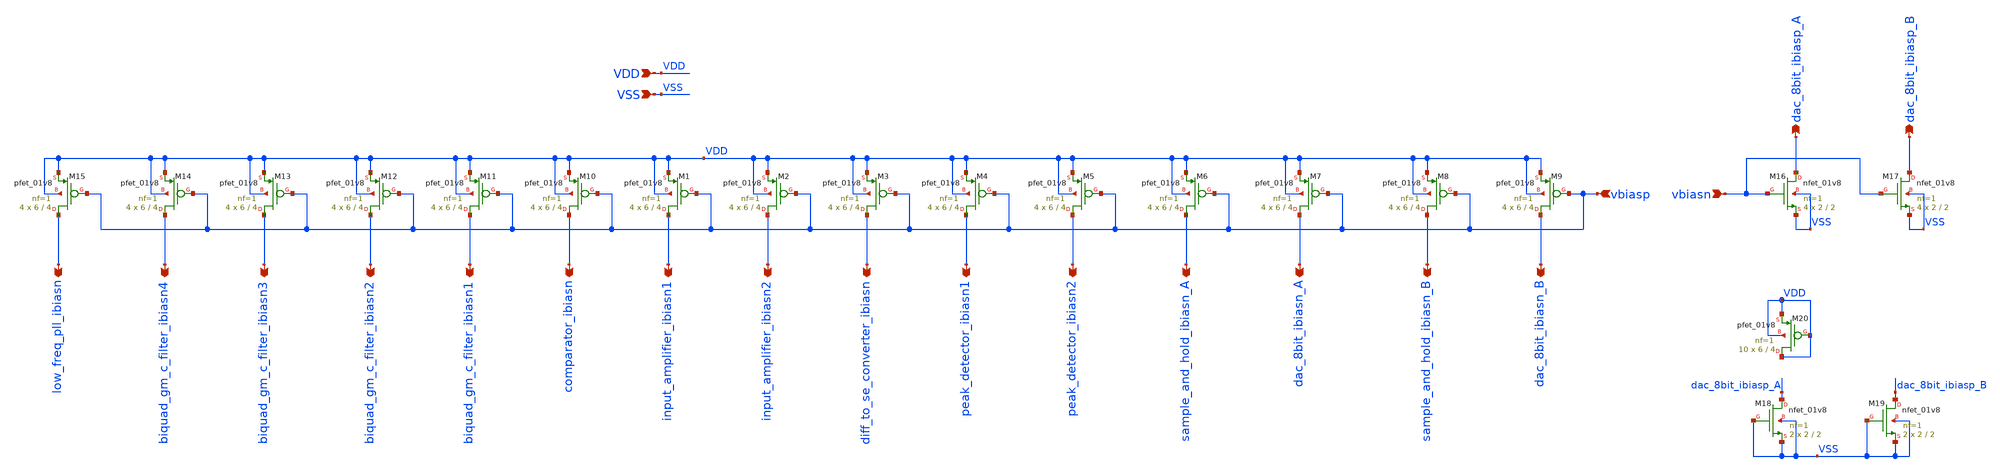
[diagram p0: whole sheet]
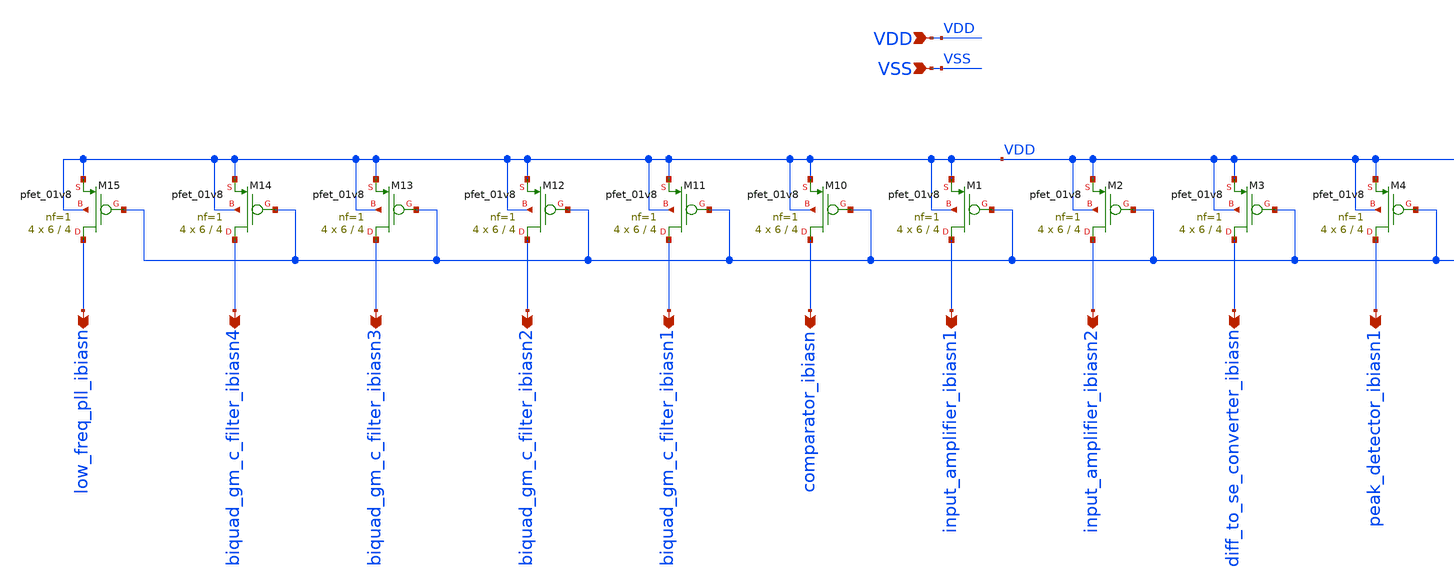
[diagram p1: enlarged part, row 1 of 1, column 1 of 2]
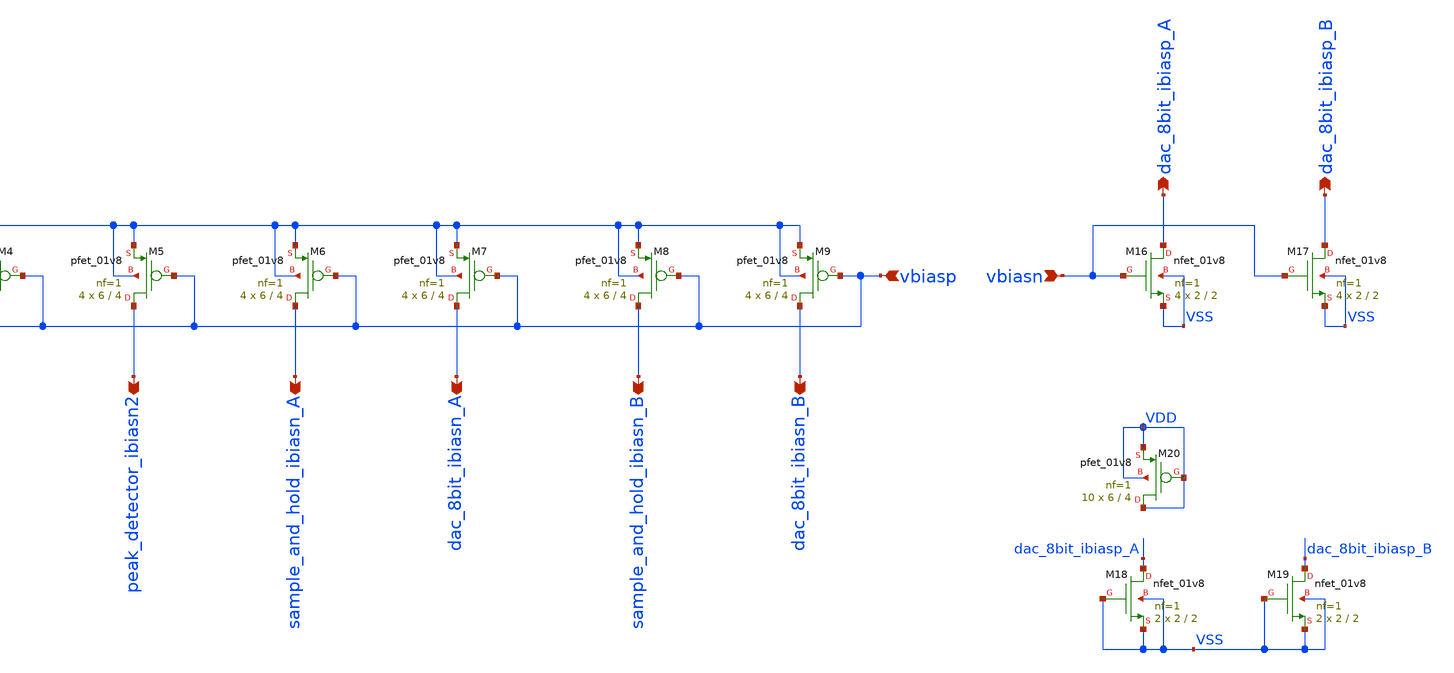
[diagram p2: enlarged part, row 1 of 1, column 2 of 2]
** sch_path: designs/bias_current_distribution_lvs.sch
* Copyright 2020 Stefan Frederik Schippers
* Licensed under the Apache License, Version 2.0 (the "License");
* you may not use this file except in compliance with the License.
* You may obtain a copy of the License at
* https://www.apache.org/licenses/LICENSE-2.0
* Unless required by applicable law or agreed to in writing, software
* distributed under the License is distributed on an "AS IS" BASIS,
* WITHOUT WARRANTIES OR CONDITIONS OF ANY KIND, either express or implied.
* See the License for the specific language governing permissions and
* limitations under the License.
**.subckt bias_current_distribution_lvs VDD VSS vbiasp input_amplifier_ibiasn1
*+ input_amplifier_ibiasn2 diff_to_se_converter_ibiasn peak_detector_ibiasn1 peak_detector_ibiasn2 sample_and_hold_ibiasn_A
*+ dac_8bit_ibiasn_A sample_and_hold_ibiasn_B dac_8bit_ibiasn_B comparator_ibiasn biquad_gm_c_filter_ibiasn1
*+ biquad_gm_c_filter_ibiasn2 biquad_gm_c_filter_ibiasn3 biquad_gm_c_filter_ibiasn4 low_freq_pll_ibiasn vbiasn dac_8bit_ibiasp_A
*+ dac_8bit_ibiasp_B
*.ipin VDD
*.ipin VSS
*.ipin vbiasp
*.opin input_amplifier_ibiasn1
*.opin input_amplifier_ibiasn2
*.opin diff_to_se_converter_ibiasn
*.opin peak_detector_ibiasn1
*.opin peak_detector_ibiasn2
*.opin sample_and_hold_ibiasn_A
*.opin dac_8bit_ibiasn_A
*.opin sample_and_hold_ibiasn_B
*.opin dac_8bit_ibiasn_B
*.opin comparator_ibiasn
*.opin biquad_gm_c_filter_ibiasn1
*.opin biquad_gm_c_filter_ibiasn2
*.opin biquad_gm_c_filter_ibiasn3
*.opin biquad_gm_c_filter_ibiasn4
*.opin low_freq_pll_ibiasn
*.ipin vbiasn
*.opin dac_8bit_ibiasp_A
*.opin dac_8bit_ibiasp_B
XM1 input_amplifier_ibiasn1 vbiasp VDD VDD sky130_fd_pr__pfet_01v8 L=4 W=6 nf=1 ad='int((nf+1)/2) * W/nf * 0.29'
+ as='int((nf+2)/2) * W/nf * 0.29' pd='2*int((nf+1)/2) * (W/nf + 0.29)' ps='2*int((nf+2)/2) * (W/nf + 0.29)'
+ nrd='0.29 / W' nrs='0.29 / W' sa=0 sb=0 sd=0 mult=4 m=4
XM2 input_amplifier_ibiasn2 vbiasp VDD VDD sky130_fd_pr__pfet_01v8 L=4 W=6 nf=1 ad='int((nf+1)/2) * W/nf * 0.29'
+ as='int((nf+2)/2) * W/nf * 0.29' pd='2*int((nf+1)/2) * (W/nf + 0.29)' ps='2*int((nf+2)/2) * (W/nf + 0.29)'
+ nrd='0.29 / W' nrs='0.29 / W' sa=0 sb=0 sd=0 mult=4 m=4
XM3 diff_to_se_converter_ibiasn vbiasp VDD VDD sky130_fd_pr__pfet_01v8 L=4 W=6 nf=1 ad='int((nf+1)/2) * W/nf * 0.29'
+ as='int((nf+2)/2) * W/nf * 0.29' pd='2*int((nf+1)/2) * (W/nf + 0.29)' ps='2*int((nf+2)/2) * (W/nf + 0.29)'
+ nrd='0.29 / W' nrs='0.29 / W' sa=0 sb=0 sd=0 mult=4 m=4
XM4 peak_detector_ibiasn1 vbiasp VDD VDD sky130_fd_pr__pfet_01v8 L=4 W=6 nf=1 ad='int((nf+1)/2) * W/nf * 0.29'
+ as='int((nf+2)/2) * W/nf * 0.29' pd='2*int((nf+1)/2) * (W/nf + 0.29)' ps='2*int((nf+2)/2) * (W/nf + 0.29)'
+ nrd='0.29 / W' nrs='0.29 / W' sa=0 sb=0 sd=0 mult=4 m=4
XM5 peak_detector_ibiasn2 vbiasp VDD VDD sky130_fd_pr__pfet_01v8 L=4 W=6 nf=1 ad='int((nf+1)/2) * W/nf * 0.29'
+ as='int((nf+2)/2) * W/nf * 0.29' pd='2*int((nf+1)/2) * (W/nf + 0.29)' ps='2*int((nf+2)/2) * (W/nf + 0.29)'
+ nrd='0.29 / W' nrs='0.29 / W' sa=0 sb=0 sd=0 mult=4 m=4
XM6 sample_and_hold_ibiasn_A vbiasp VDD VDD sky130_fd_pr__pfet_01v8 L=4 W=6 nf=1 ad='int((nf+1)/2) * W/nf * 0.29'
+ as='int((nf+2)/2) * W/nf * 0.29' pd='2*int((nf+1)/2) * (W/nf + 0.29)' ps='2*int((nf+2)/2) * (W/nf + 0.29)'
+ nrd='0.29 / W' nrs='0.29 / W' sa=0 sb=0 sd=0 mult=4 m=4
XM7 dac_8bit_ibiasn_A vbiasp VDD VDD sky130_fd_pr__pfet_01v8 L=4 W=6 nf=1 ad='int((nf+1)/2) * W/nf * 0.29'
+ as='int((nf+2)/2) * W/nf * 0.29' pd='2*int((nf+1)/2) * (W/nf + 0.29)' ps='2*int((nf+2)/2) * (W/nf + 0.29)'
+ nrd='0.29 / W' nrs='0.29 / W' sa=0 sb=0 sd=0 mult=4 m=4
XM8 sample_and_hold_ibiasn_B vbiasp VDD VDD sky130_fd_pr__pfet_01v8 L=4 W=6 nf=1 ad='int((nf+1)/2) * W/nf * 0.29'
+ as='int((nf+2)/2) * W/nf * 0.29' pd='2*int((nf+1)/2) * (W/nf + 0.29)' ps='2*int((nf+2)/2) * (W/nf + 0.29)'
+ nrd='0.29 / W' nrs='0.29 / W' sa=0 sb=0 sd=0 mult=4 m=4
XM9 dac_8bit_ibiasn_B vbiasp VDD VDD sky130_fd_pr__pfet_01v8 L=4 W=6 nf=1 ad='int((nf+1)/2) * W/nf * 0.29'
+ as='int((nf+2)/2) * W/nf * 0.29' pd='2*int((nf+1)/2) * (W/nf + 0.29)' ps='2*int((nf+2)/2) * (W/nf + 0.29)'
+ nrd='0.29 / W' nrs='0.29 / W' sa=0 sb=0 sd=0 mult=4 m=4
XM10 comparator_ibiasn vbiasp VDD VDD sky130_fd_pr__pfet_01v8 L=4 W=6 nf=1 ad='int((nf+1)/2) * W/nf * 0.29'
+ as='int((nf+2)/2) * W/nf * 0.29' pd='2*int((nf+1)/2) * (W/nf + 0.29)' ps='2*int((nf+2)/2) * (W/nf + 0.29)'
+ nrd='0.29 / W' nrs='0.29 / W' sa=0 sb=0 sd=0 mult=4 m=4
XM11 biquad_gm_c_filter_ibiasn1 vbiasp VDD VDD sky130_fd_pr__pfet_01v8 L=4 W=6 nf=1 ad='int((nf+1)/2) * W/nf * 0.29'
+ as='int((nf+2)/2) * W/nf * 0.29' pd='2*int((nf+1)/2) * (W/nf + 0.29)' ps='2*int((nf+2)/2) * (W/nf + 0.29)'
+ nrd='0.29 / W' nrs='0.29 / W' sa=0 sb=0 sd=0 mult=4 m=4
XM12 biquad_gm_c_filter_ibiasn2 vbiasp VDD VDD sky130_fd_pr__pfet_01v8 L=4 W=6 nf=1 ad='int((nf+1)/2) * W/nf * 0.29'
+ as='int((nf+2)/2) * W/nf * 0.29' pd='2*int((nf+1)/2) * (W/nf + 0.29)' ps='2*int((nf+2)/2) * (W/nf + 0.29)'
+ nrd='0.29 / W' nrs='0.29 / W' sa=0 sb=0 sd=0 mult=4 m=4
XM13 biquad_gm_c_filter_ibiasn3 vbiasp VDD VDD sky130_fd_pr__pfet_01v8 L=4 W=6 nf=1 ad='int((nf+1)/2) * W/nf * 0.29'
+ as='int((nf+2)/2) * W/nf * 0.29' pd='2*int((nf+1)/2) * (W/nf + 0.29)' ps='2*int((nf+2)/2) * (W/nf + 0.29)'
+ nrd='0.29 / W' nrs='0.29 / W' sa=0 sb=0 sd=0 mult=4 m=4
XM14 biquad_gm_c_filter_ibiasn4 vbiasp VDD VDD sky130_fd_pr__pfet_01v8 L=4 W=6 nf=1 ad='int((nf+1)/2) * W/nf * 0.29'
+ as='int((nf+2)/2) * W/nf * 0.29' pd='2*int((nf+1)/2) * (W/nf + 0.29)' ps='2*int((nf+2)/2) * (W/nf + 0.29)'
+ nrd='0.29 / W' nrs='0.29 / W' sa=0 sb=0 sd=0 mult=4 m=4
XM15 low_freq_pll_ibiasn vbiasp VDD VDD sky130_fd_pr__pfet_01v8 L=4 W=6 nf=1 ad='int((nf+1)/2) * W/nf * 0.29'
+ as='int((nf+2)/2) * W/nf * 0.29' pd='2*int((nf+1)/2) * (W/nf + 0.29)' ps='2*int((nf+2)/2) * (W/nf + 0.29)'
+ nrd='0.29 / W' nrs='0.29 / W' sa=0 sb=0 sd=0 mult=4 m=4
XM16 dac_8bit_ibiasp_A vbiasn VSS VSS sky130_fd_pr__nfet_01v8 L=2 W=2 nf=1 ad='int((nf+1)/2) * W/nf * 0.29'
+ as='int((nf+2)/2) * W/nf * 0.29' pd='2*int((nf+1)/2) * (W/nf + 0.29)' ps='2*int((nf+2)/2) * (W/nf + 0.29)'
+ nrd='0.29 / W' nrs='0.29 / W' sa=0 sb=0 sd=0 mult=4 m=4
XM17 dac_8bit_ibiasp_B vbiasn VSS VSS sky130_fd_pr__nfet_01v8 L=2 W=2 nf=1 ad='int((nf+1)/2) * W/nf * 0.29'
+ as='int((nf+2)/2) * W/nf * 0.29' pd='2*int((nf+1)/2) * (W/nf + 0.29)' ps='2*int((nf+2)/2) * (W/nf + 0.29)'
+ nrd='0.29 / W' nrs='0.29 / W' sa=0 sb=0 sd=0 mult=4 m=4
XM18 dac_8bit_ibiasp_A VSS VSS VSS sky130_fd_pr__nfet_01v8 L=2 W=2 nf=1 ad='int((nf+1)/2) * W/nf * 0.29'
+ as='int((nf+2)/2) * W/nf * 0.29' pd='2*int((nf+1)/2) * (W/nf + 0.29)' ps='2*int((nf+2)/2) * (W/nf + 0.29)'
+ nrd='0.29 / W' nrs='0.29 / W' sa=0 sb=0 sd=0 mult=2 m=2
XM19 dac_8bit_ibiasp_B VSS VSS VSS sky130_fd_pr__nfet_01v8 L=2 W=2 nf=1 ad='int((nf+1)/2) * W/nf * 0.29'
+ as='int((nf+2)/2) * W/nf * 0.29' pd='2*int((nf+1)/2) * (W/nf + 0.29)' ps='2*int((nf+2)/2) * (W/nf + 0.29)'
+ nrd='0.29 / W' nrs='0.29 / W' sa=0 sb=0 sd=0 mult=2 m=2
XM20 VDD VDD VDD VDD sky130_fd_pr__pfet_01v8 L=4 W=6 nf=1 ad='int((nf+1)/2) * W/nf * 0.29' as='int((nf+2)/2) * W/nf * 0.29'
+ pd='2*int((nf+1)/2) * (W/nf + 0.29)' ps='2*int((nf+2)/2) * (W/nf + 0.29)' nrd='0.29 / W' nrs='0.29 / W'
+ sa=0 sb=0 sd=0 mult=10 m=10
**.ends
.end
